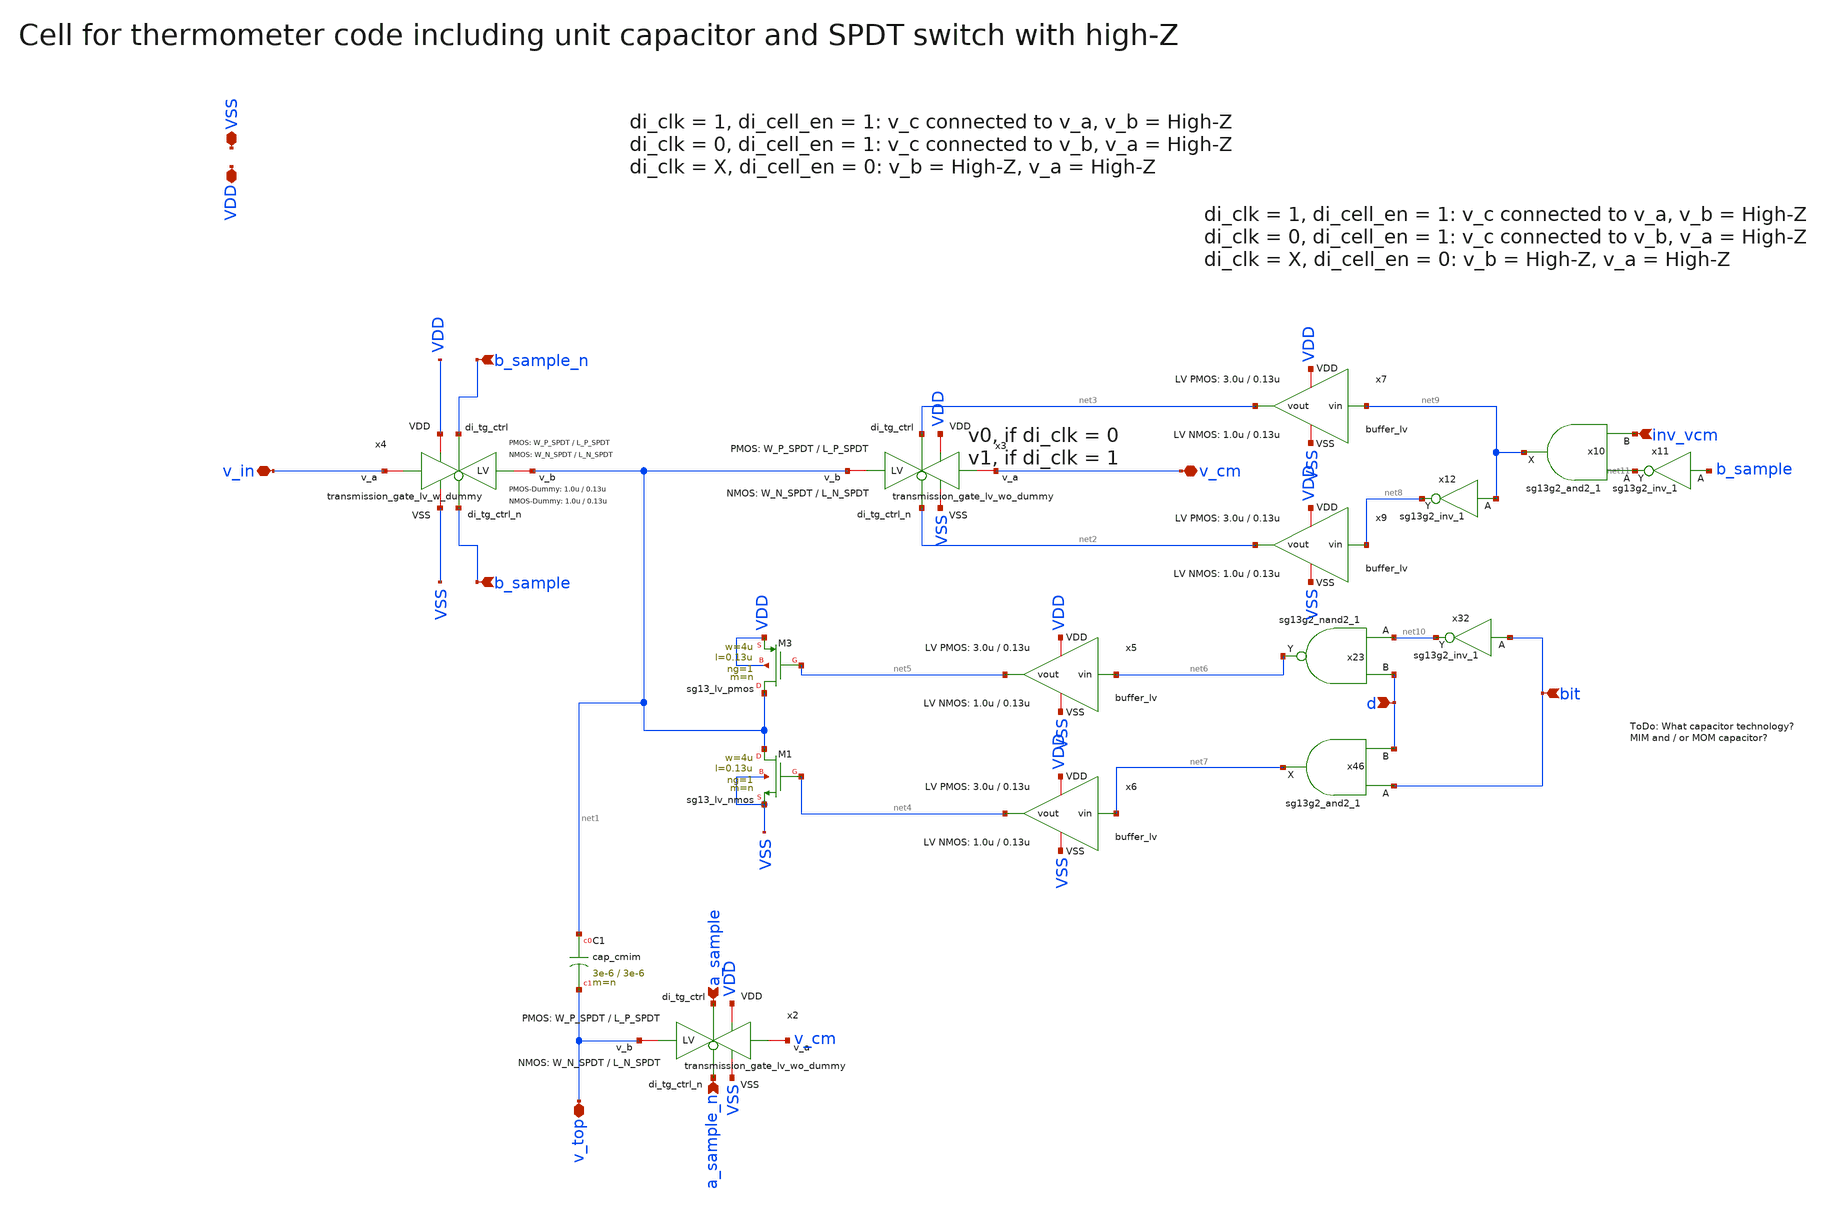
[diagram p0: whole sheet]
** sch_path: xschem/dac_icms_cell/unit_cell.sch
**.subckt unit_cell v_top a_sample a_sample_n b_sample b_sample_n v_in d v_cm bit inv_vcm VSS VDD
*.iopin v_top
*.ipin a_sample
*.ipin a_sample_n
*.ipin b_sample
*.ipin b_sample_n
*.iopin v_in
*.ipin d
*.iopin v_cm
*.ipin bit
*.ipin inv_vcm
*.iopin VSS
*.iopin VDD
x2 VDD a_sample VSS v_top v_cm a_sample_n transmission_gate_lv_wo_dummy W_P=W_P_SPDT L_P=L_P_SPDT
+ W_N=W_N_SPDT L_N=L_N_SPDT W_P_D=1.0u L_P_D=0.13u W_N_D=1.0u L_N_D=0.13u n=n
XC1 net1 v_top cap_cmim w=3e-6 l=3e-6 m=n mm_ok=1
XM1 net1 net4 VSS VSS sg13_lv_nmos w=4u l=0.13u ng=1 m=n mm_ok=1
XM3 net1 net5 VDD VDD sg13_lv_pmos w=4u l=0.13u ng=1 m=n mm_ok=1
x3 VDD net3 VSS net1 v_cm net2 transmission_gate_lv_wo_dummy W_P=W_P_SPDT L_P=L_P_SPDT W_N=W_N_SPDT
+ L_N=L_N_SPDT W_P_D=1.0u L_P_D=0.13u W_N_D=1.0u L_N_D=0.13u n=n
x4 VDD b_sample_n VSS net1 v_in b_sample transmission_gate_lv_w_dummy W_P=W_P_SPDT L_P=L_P_SPDT
+ W_N=W_N_SPDT L_N=L_N_SPDT W_P_D=1.0u L_P_D=0.13u W_N_D=1.0u L_N_D=0.13u n=n
x23 net6 net10 d VDD VSS sg13g2_nand2_1
x46 net7 bit d VDD VSS sg13g2_and2_1
x5 VDD net6 net5 VSS buffer_lv W_P_INV=3.0u L_P_INV=0.13u W_N_INV=1.0u L_N_INV=0.13u
x6 VDD net7 net4 VSS buffer_lv W_P_INV=3.0u L_P_INV=0.13u W_N_INV=1.0u L_N_INV=0.13u
x7 VDD net9 net3 VSS buffer_lv W_P_INV=3.0u L_P_INV=0.13u W_N_INV=1.0u L_N_INV=0.13u
x9 VDD net8 net2 VSS buffer_lv W_P_INV=3.0u L_P_INV=0.13u W_N_INV=1.0u L_N_INV=0.13u
x32 net10 bit VDD VSS sg13g2_inv_1
x10 net9 net11 inv_vcm VDD VSS sg13g2_and2_1
x11 net11 b_sample VDD VSS sg13g2_inv_1
x12 net8 net9 VDD VSS sg13g2_inv_1
**.ends

* expanding   symbol:  transmission_gate/transmission_gate_lv_wo_dummy.sym # of pins=6
** sym_path: xschem/transmission_gate/transmission_gate_lv_wo_dummy.sym
** sch_path: xschem/transmission_gate/transmission_gate_lv_wo_dummy.sch
.subckt transmission_gate_lv_wo_dummy VDD di_tg_ctrl VSS v_b v_a di_tg_ctrl_n  W_P=2.0u L_P=0.13u
+ W_N=2.0u L_N=0.13u W_P_D=1.0u L_P_D=0.13u W_N_D=1.0u L_N_D=0.13u n=1
*.iopin v_a
*.iopin v_b
*.iopin VDD
*.iopin VSS
*.ipin di_tg_ctrl
*.ipin di_tg_ctrl_n
XM1 v_a di_tg_ctrl v_b VSS sg13_lv_nmos w=W_N l=L_N ng=1 m=n mm_ok=1
XM2 v_a di_tg_ctrl_n v_b VDD sg13_lv_pmos w=W_P l=L_P ng=1 m=n mm_ok=1
.ends


* expanding   symbol:  transmission_gate/transmission_gate_lv_w_dummy.sym # of pins=6
** sym_path: xschem/transmission_gate/transmission_gate_lv_w_dummy.sym
** sch_path: xschem/transmission_gate/transmission_gate_lv_w_dummy.sch
.subckt transmission_gate_lv_w_dummy VDD di_tg_ctrl VSS v_b v_a di_tg_ctrl_n  W_P=2.0u L_P=0.13u
+ W_N=2.0u L_N=0.13u W_P_D=1.0u L_P_D=0.13u W_N_D=1.0u L_N_D=0.13u n=1
*.iopin v_a
*.iopin v_b
*.iopin VDD
*.iopin VSS
*.ipin di_tg_ctrl
*.ipin di_tg_ctrl_n
XM1 v_a di_tg_ctrl v_b VSS sg13_lv_nmos w=W_N l=L_N ng=1 m=n mm_ok=1
XM2 v_a di_tg_ctrl_n v_b VDD sg13_lv_pmos w=W_P l=L_P ng=1 m=n mm_ok=1
XMdummy2 v_b di_tg_ctrl v_b VDD sg13_lv_pmos w=W_P l=L_P ng=1 m={n/2} mm_ok=1
XMdummy1 v_b di_tg_ctrl_n v_b VSS sg13_lv_nmos w=W_N l=L_N ng=1 m={n/2} mm_ok=1
.ends


* expanding   symbol:  sg13g2_stdcells/sg13g2_nand2_1.sym # of pins=3
** sym_path: sg13g2_stdcells/sg13g2_nand2_1.sym
** sch_path: sg13g2_stdcells/sg13g2_nand2_1.sch
.subckt sg13g2_nand2_1 Y A B VDD VSS
*.iopin VDD
*.iopin VSS
*.ipin A
*.ipin B
*.opin Y
XM1 Y A net1 VSS sg13_lv_nmos w=740.00n l=130.00n ng=1 m=1 mm_ok=1
XM2 net1 B VSS VSS sg13_lv_nmos w=740.00n l=130.00n ng=1 m=1 mm_ok=1
XM3 Y A VDD VDD sg13_lv_pmos w=1.12u l=130.00n ng=1 m=1 mm_ok=1
XM4 Y B VDD VDD sg13_lv_pmos w=1.12u l=130.00n ng=1 m=1 mm_ok=1
.ends


* expanding   symbol:  sg13g2_stdcells/sg13g2_and2_1.sym # of pins=3
** sym_path: sg13g2_stdcells/sg13g2_and2_1.sym
** sch_path: sg13g2_stdcells/sg13g2_and2_1.sch
.subckt sg13g2_and2_1 X A B VDD VSS
*.ipin A
*.ipin B
*.opin X
*.iopin VDD
*.iopin VSS
XM1 net1 A net2 VSS sg13_lv_nmos w=640.00n l=130.00n ng=1 m=1 mm_ok=1
XM2 net2 B VSS VSS sg13_lv_nmos w=640.00n l=130.00n ng=1 m=1 mm_ok=1
XM3 X net1 VSS VSS sg13_lv_nmos w=740.00n l=130.00n ng=1 m=1 mm_ok=1
XM4 net1 B VDD VDD sg13_lv_pmos w=840.00n l=130.00n ng=1 m=1 mm_ok=1
XM5 net1 A VDD VDD sg13_lv_pmos w=840.00n l=130.00n ng=1 m=1 mm_ok=1
XM6 X net1 VDD VDD sg13_lv_pmos w=1.12u l=130.00n ng=1 m=1 mm_ok=1
.ends


* expanding   symbol:  buffer/buffer_lv.sym # of pins=4
** sym_path: buffer/buffer_lv.sym
** sch_path: buffer/buffer_lv.sch
.subckt buffer_lv VDD vin vout VSS  W_P_INV=3.0u L_P_INV=0.13u W_N_INV=1.0u L_N_INV=0.13u
*.ipin vin
*.iopin VDD
*.iopin VSS
*.opin vout
x1 VDD vin net1 VSS inverter_lv W_P=W_P_INV L_P=L_P_INV W_N=W_N_INV L_N=L_N_INV N_C=1
x2 VDD net1 vout VSS inverter_lv W_P=W_P_INV L_P=L_P_INV W_N=W_N_INV L_N=L_N_INV N_C=1
.ends


* expanding   symbol:  sg13g2_stdcells/sg13g2_inv_1.sym # of pins=2
** sym_path: sg13g2_stdcells/sg13g2_inv_1.sym
** sch_path: sg13g2_stdcells/sg13g2_inv_1.sch
.subckt sg13g2_inv_1 Y A VDD VSS
*.opin Y
*.ipin A
*.iopin VDD
*.iopin VSS
XM1 Y A VSS VSS sg13_lv_nmos w=740.00n l=130.00n ng=1 m=1 mm_ok=1
XM2 Y A VDD VDD sg13_lv_pmos w=1.12u l=130.00n ng=1 m=1 mm_ok=1
.ends


* expanding   symbol:  inverter/inverter_lv.sym # of pins=4
** sym_path: xschem/inverter/inverter_lv.sym
** sch_path: xschem/inverter/inverter_lv.sch
.subckt inverter_lv VDD vin vout VSS  W_P=3.0u L_P=0.13u W_N=1.0u L_N=0.13u N_C=1
*.ipin vin
*.iopin VDD
*.iopin VSS
*.opin vout
XM1 vout vin VDD VDD sg13_lv_pmos w=W_P l=L_P ng=1 m={N_C} mm_ok=1
XM2 vout vin VSS VSS sg13_lv_nmos w=W_N l=L_N ng=1 m={N_C} mm_ok=1
.ends

.end
